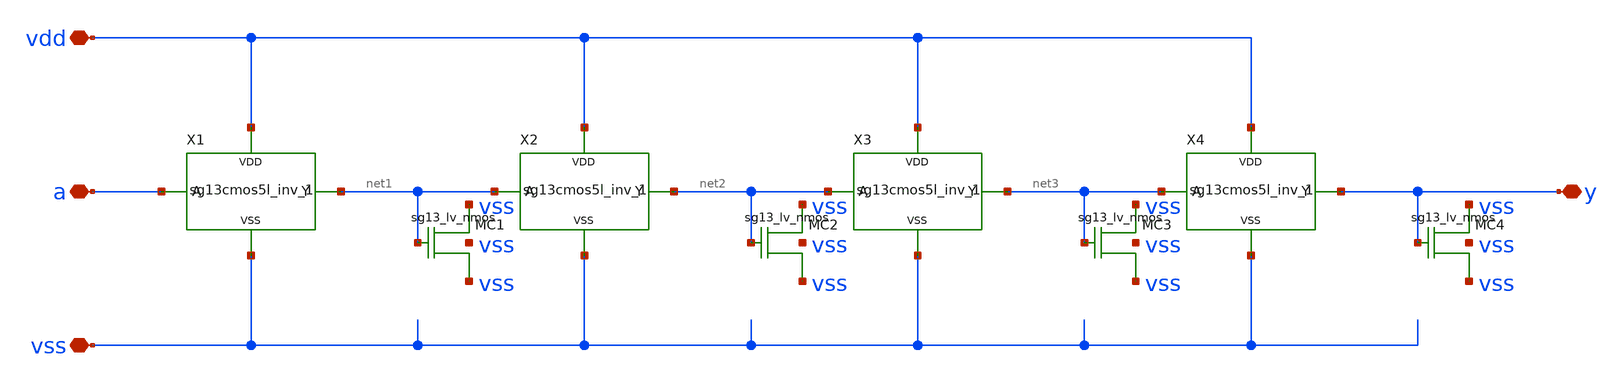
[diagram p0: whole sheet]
** sch_path: xschem/schematics/delay_2ns.sch
**.subckt delay_2ns a y vdd vss
*.iopin a
*.iopin y
*.iopin vdd
*.iopin vss
X1 net1 a vdd vss sg13cmos5l_inv_1
XMC1 vss net1 vss vss sg13_lv_nmos w=7.4u l=6u ng=1 m=1
X2 net2 net1 vdd vss sg13cmos5l_inv_1
XMC2 vss net2 vss vss sg13_lv_nmos w=7.4u l=6u ng=1 m=1
X3 net3 net2 vdd vss sg13cmos5l_inv_1
XMC3 vss net3 vss vss sg13_lv_nmos w=7.4u l=6u ng=1 m=1
X4 y net3 vdd vss sg13cmos5l_inv_1
XMC4 vss y vss vss sg13_lv_nmos w=3.2u l=6u ng=1 m=1
**.ends

* expanding   symbol:  logic_gates/sg13cmos5l_inv_1.sym # of pins=4
** sym_path: xschem/logic_gates/sg13cmos5l_inv_1.sym
** sch_path: xschem/logic_gates/sg13cmos5l_inv_1.sch
.subckt sg13cmos5l_inv_1 Y A VDD VSS
*.iopin Y
*.iopin A
*.iopin VDD
*.iopin VSS
XMN0 Y A VSS VSS sg13_lv_nmos w=0.74u l=0.13u ng=1 m=1
XMP0 VDD A Y VDD sg13_lv_pmos w=1.12u l=0.13u ng=1 m=1
.ends

.end
